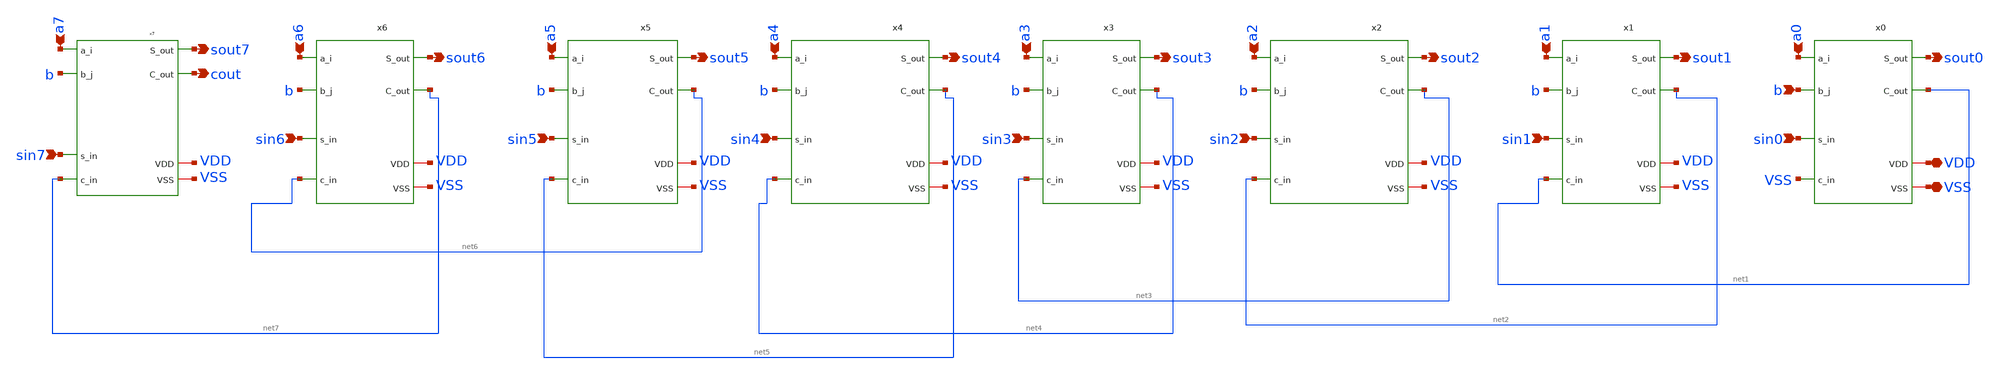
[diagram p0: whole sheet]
** sch_path: xschem/row_7.sch
**.subckt row_7 a0 a1 a2 a3 a4 a5 a6 a7 b sin0 sin1 sin2 sin3 sin4 sin5 sin6 sin7 sout1 sout2 sout3
*+ sout4 sout5 sout6 sout7 sout0 cout VDD VSS
*.ipin a0
*.ipin a1
*.ipin a2
*.ipin a3
*.ipin a4
*.ipin a5
*.ipin a6
*.ipin a7
*.ipin b
*.ipin sin0
*.ipin sin1
*.ipin sin2
*.ipin sin3
*.ipin sin4
*.ipin sin5
*.ipin sin6
*.ipin sin7
*.opin sout1
*.opin sout2
*.opin sout3
*.opin sout4
*.opin sout5
*.opin sout6
*.opin sout7
*.opin sout0
*.opin cout
*.iopin VDD
*.iopin VSS
x7 sout7 a7 b VDD VSS cout sin7 net7 pp_cell
x6 sout6 a6 b VDD VSS net7 sin6 net6 pp_cell_sign
x2 sout2 a2 b VDD VSS net3 sin2 net2 pp_cell_sign
x3 sout3 a3 b VDD VSS net4 sin3 net3 pp_cell_sign
x4 sout4 a4 b VDD VSS net5 sin4 net4 pp_cell_sign
x5 sout5 a5 b VDD VSS net6 sin5 net5 pp_cell_sign
x0 sout0 a0 b VDD VSS net1 sin0 VSS pp_cell_sign
x1 sout1 a1 b VDD VSS net2 sin1 net1 pp_cell_sign
**.ends
.end
